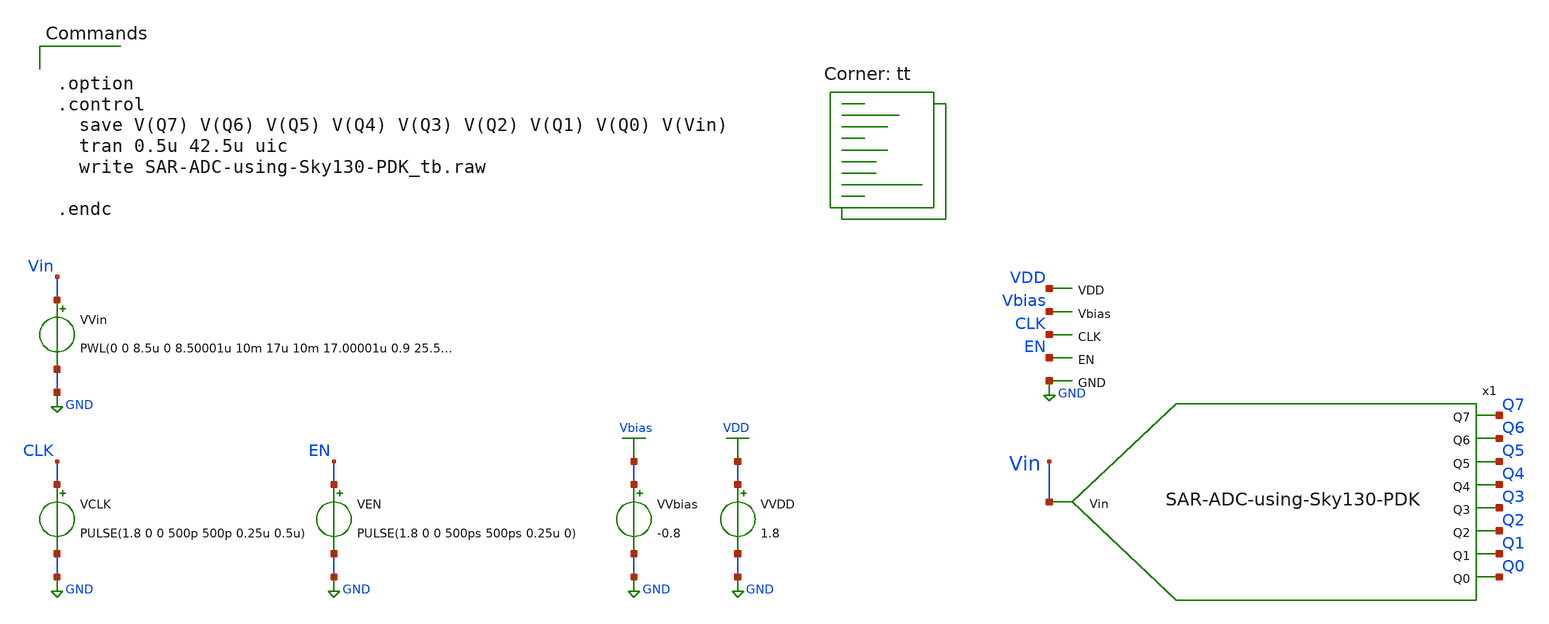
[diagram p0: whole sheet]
** sch_path: xschem/SAR-ADC-using-Sky130-PDK_tb.sch
**.subckt SAR-ADC-using-Sky130-PDK_tb
x1 VDD Vin Q0 Vbias EN Q1 CLK Q2 Q3 Q4 Q5 Q6 Q7 GND SAR-ADC-using-Sky130-PDK
VCLK CLK GND PULSE(1.8 0 0 500p 500p 0.25u 0.5u)
VVDD VDD GND 1.8
VEN EN GND PULSE(1.8 0 0 500ps 500ps 0.25u 0)
VVbias Vbias GND -0.8
VVin Vin GND PWL(0 0 8.5u 0 8.50001u 10m 17u 10m 17.00001u 0.9 25.5u 0.9 25.50001u 1.7 34u 1.7
+ 34.00001u 1.8 42.5u 1.8
**** begin user architecture code


.option
.control
  save V(Q7) V(Q6) V(Q5) V(Q4) V(Q3) V(Q2) V(Q1) V(Q0) V(Vin)
  tran 0.5u 42.5u uic
  write SAR-ADC-using-Sky130-PDK_tb.raw

.endc


.lib $::SKYWATER_MODELS/sky130.lib.spice tt
**** end user architecture code
**.ends
.GLOBAL GND
.GLOBAL VDD
.GLOBAL Vbias
.end
